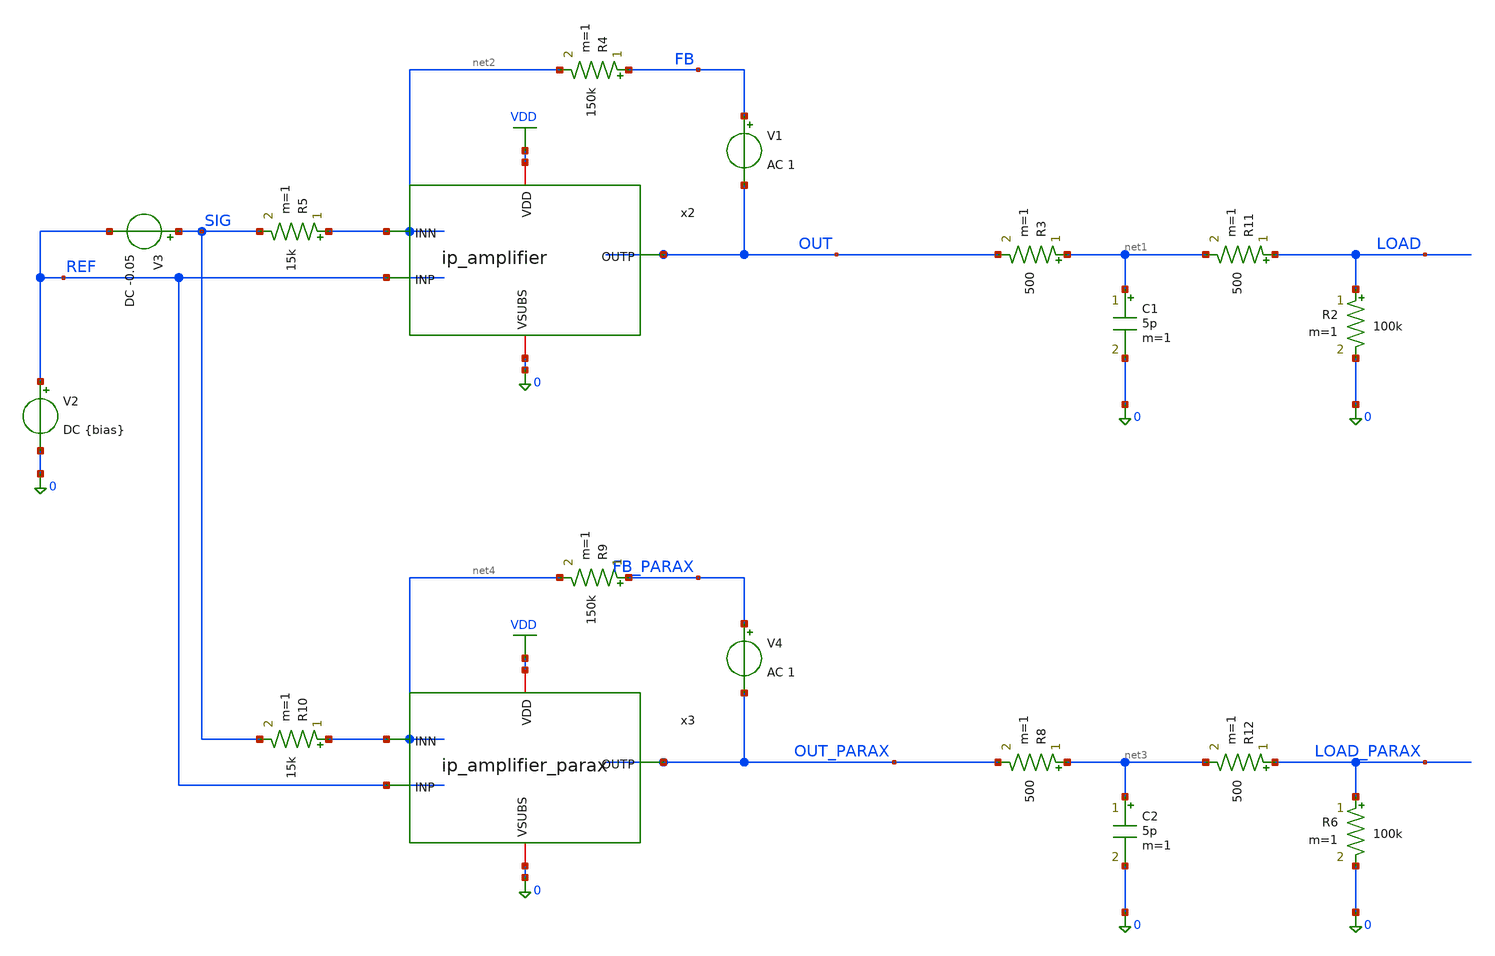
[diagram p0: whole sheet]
** sch_path: xschem/tb_amplifier_x10_ac.sch
**.subckt tb_amplifier_x10_ac
V2 REF 0 DC {bias}
x2 VDD OUT REF net2 0 ip_amplifier
R2 LOAD 0 100k m=1
V1 FB OUT AC 1
R3 net1 OUT 500 m=1
C1 net1 0 5p m=1
R4 FB net2 150k m=1
R5 net2 SIG 15k m=1
V3 SIG REF DC -0.05
R6 LOAD_PARAX 0 100k m=1
V4 FB_PARAX OUT_PARAX AC 1
R8 net3 OUT_PARAX 500 m=1
C2 net3 0 5p m=1
R9 FB_PARAX net4 150k m=1
R10 net4 SIG 15k m=1
x3 VDD OUT_PARAX REF net4 0 ip_amplifier_parax
R11 LOAD net1 500 m=1
R12 LOAD_PARAX net3 500 m=1
**** begin user architecture code

.lib $::180MCU_MODELS/sm141064.ngspice statistical
.lib $::180MCU_MODELS/sm141064.ngspice res_statistical
.lib $::180MCU_MODELS/sm141064.ngspice moscap_typical
.lib $::180MCU_MODELS/sm141064.ngspice diode_typical




V_DD VDD 0 3.3

# Global parameters typically sourced from design.ngspice
.param sw_stat_global   = 1
.param sw_stat_mismatch = 1
.param mc_skew          = 1
.param res_mc_skew=3
.param cap_mc_skew=3
.param fnoicor=0

.param bias=1.0

.control
	op
	write tb_amplifier_x10_ac.op.raw
  	foreach v_bias 0.5 1.0 1.5
    		alterparam bias=$v_bias
		repeat 10
			mc_source
			ac dec 1000 1000 1e9
			let oltf = v(out) / v(fb)
			let oltf_parax = v(out_parax) / v(fb_parax)
			write tb_amplifier_x10_ac.raw
			set appendwrite
			reset
		end
	end
	quit
.endc



**** end user architecture code
**.ends

* expanding   symbol:  ip_amplifier.sym # of pins=5
** sym_path: xschem/ip_amplifier.sym
** sch_path: xschem/ip_amplifier.sch
.subckt ip_amplifier VDD OUTP INP INN VSUBS
*.iopin VDD
*.iopin VSUBS
*.ipin INP
*.ipin INN
*.opin OUTP
XM1 net10 INP net8 VDD pfet_06v0 L=0.7u W=11.0u nf=1 ad='int((nf+1)/2) * W/nf * 0.18u' as='int((nf+2)/2) * W/nf * 0.18u'
+ pd='2*int((nf+1)/2) * (W/nf + 0.18u)' ps='2*int((nf+2)/2) * (W/nf + 0.18u)' nrd='0.18u / W' nrs='0.18u / W'
+ sa=0 sb=0 sd=0 m=2 par=2
XM2 net9 INN net8 VDD pfet_06v0 L=0.7u W=11.0u nf=1 ad='int((nf+1)/2) * W/nf * 0.18u' as='int((nf+2)/2) * W/nf * 0.18u'
+ pd='2*int((nf+1)/2) * (W/nf + 0.18u)' ps='2*int((nf+2)/2) * (W/nf + 0.18u)' nrd='0.18u / W' nrs='0.18u / W'
+ sa=0 sb=0 sd=0 m=2 par=2
XM5 net10 net1 VSUBS vsubs nfet_06v0 L=2u W=5u nf=1 ad='int((nf+1)/2) * W/nf * 0.18u' as='int((nf+2)/2) * W/nf * 0.18u'
+ pd='2*int((nf+1)/2) * (W/nf + 0.18u)' ps='2*int((nf+2)/2) * (W/nf + 0.18u)' nrd='0.18u / W' nrs='0.18u / W'
+ sa=0 sb=0 sd=0 m=1 par=1
XM6 net9 net1 VSUBS vsubs nfet_06v0 L=2u W=5u nf=1 ad='int((nf+1)/2) * W/nf * 0.18u' as='int((nf+2)/2) * W/nf * 0.18u'
+ pd='2*int((nf+1)/2) * (W/nf + 0.18u)' ps='2*int((nf+2)/2) * (W/nf + 0.18u)' nrd='0.18u / W' nrs='0.18u / W'
+ sa=0 sb=0 sd=0 m=1 par=1
XM3 net3 net1 VSUBS vsubs nfet_06v0 L=1u W=12.5u nf=1 ad='int((nf+1)/2) * W/nf * 0.18u' as='int((nf+2)/2) * W/nf * 0.18u'
+ pd='2*int((nf+1)/2) * (W/nf + 0.18u)' ps='2*int((nf+2)/2) * (W/nf + 0.18u)' nrd='0.18u / W' nrs='0.18u / W'
+ sa=0 sb=0 sd=0 m=2 par=2
XM4 net2 net1 VSUBS vsubs nfet_06v0 L=1u W=5u nf=1 ad='int((nf+1)/2) * W/nf * 0.18u' as='int((nf+2)/2) * W/nf * 0.18u'
+ pd='2*int((nf+1)/2) * (W/nf + 0.18u)' ps='2*int((nf+2)/2) * (W/nf + 0.18u)' nrd='0.18u / W' nrs='0.18u / W'
+ sa=0 sb=0 sd=0 m=1 par=1
XM7 net1 net1 net3 vsubs nfet_06v0 L=0.7u W=14u nf=1 ad='int((nf+1)/2) * W/nf * 0.18u' as='int((nf+2)/2) * W/nf * 0.18u'
+ pd='2*int((nf+1)/2) * (W/nf + 0.18u)' ps='2*int((nf+2)/2) * (W/nf + 0.18u)' nrd='0.18u / W' nrs='0.18u / W'
+ sa=0 sb=0 sd=0 m=2 par=2
XM8 net4 net1 net2 vsubs nfet_06v0 L=0.7u W=14u nf=1 ad='int((nf+1)/2) * W/nf * 0.18u' as='int((nf+2)/2) * W/nf * 0.18u'
+ pd='2*int((nf+1)/2) * (W/nf + 0.18u)' ps='2*int((nf+2)/2) * (W/nf + 0.18u)' nrd='0.18u / W' nrs='0.18u / W'
+ sa=0 sb=0 sd=0 m=2 par=2
XM9 net5 net7 VDD VDD pfet_06v0 L=1u W=6u nf=1 ad='int((nf+1)/2) * W/nf * 0.18u' as='int((nf+2)/2) * W/nf * 0.18u'
+ pd='2*int((nf+1)/2) * (W/nf + 0.18u)' ps='2*int((nf+2)/2) * (W/nf + 0.18u)' nrd='0.18u / W' nrs='0.18u / W'
+ sa=0 sb=0 sd=0 m=1 par=1
XM10 net6 net7 VDD VDD pfet_06v0 L=1u W=6u nf=1 ad='int((nf+1)/2) * W/nf * 0.18u' as='int((nf+2)/2) * W/nf * 0.18u'
+ pd='2*int((nf+1)/2) * (W/nf + 0.18u)' ps='2*int((nf+2)/2) * (W/nf + 0.18u)' nrd='0.18u / W' nrs='0.18u / W'
+ sa=0 sb=0 sd=0 m=1 par=1
XM11 net7 net7 net5 VDD pfet_06v0 L=0.7u W=14u nf=1 ad='int((nf+1)/2) * W/nf * 0.18u' as='int((nf+2)/2) * W/nf * 0.18u'
+ pd='2*int((nf+1)/2) * (W/nf + 0.18u)' ps='2*int((nf+2)/2) * (W/nf + 0.18u)' nrd='0.18u / W' nrs='0.18u / W'
+ sa=0 sb=0 sd=0 m=2 par=2
XM12 net8 net7 net6 VDD pfet_06v0 L=0.7u W=14u nf=1 ad='int((nf+1)/2) * W/nf * 0.18u' as='int((nf+2)/2) * W/nf * 0.18u'
+ pd='2*int((nf+1)/2) * (W/nf + 0.18u)' ps='2*int((nf+2)/2) * (W/nf + 0.18u)' nrd='0.18u / W' nrs='0.18u / W'
+ sa=0 sb=0 sd=0 m=2 par=2
XM13 net11 net1 net9 vsubs nfet_06v0 L=0.7u W=12u nf=1 ad='int((nf+1)/2) * W/nf * 0.18u' as='int((nf+2)/2) * W/nf * 0.18u'
+ pd='2*int((nf+1)/2) * (W/nf + 0.18u)' ps='2*int((nf+2)/2) * (W/nf + 0.18u)' nrd='0.18u / W' nrs='0.18u / W'
+ sa=0 sb=0 sd=0 m=1 par=1
XM14 COMP net1 net10 vsubs nfet_06v0 L=0.7u W=12u nf=1 ad='int((nf+1)/2) * W/nf * 0.18u' as='int((nf+2)/2) * W/nf * 0.18u'
+ pd='2*int((nf+1)/2) * (W/nf + 0.18u)' ps='2*int((nf+2)/2) * (W/nf + 0.18u)' nrd='0.18u / W' nrs='0.18u / W'
+ sa=0 sb=0 sd=0 m=1 par=1
XM15 net11 net11 VDD VDD pfet_06v0 L=0.7u W=12u nf=1 ad='int((nf+1)/2) * W/nf * 0.18u' as='int((nf+2)/2) * W/nf * 0.18u'
+ pd='2*int((nf+1)/2) * (W/nf + 0.18u)' ps='2*int((nf+2)/2) * (W/nf + 0.18u)' nrd='0.18u / W' nrs='0.18u / W'
+ sa=0 sb=0 sd=0 m=1 par=1
XM16 COMP net11 VDD VDD pfet_06v0 L=0.7u W=12u nf=1 ad='int((nf+1)/2) * W/nf * 0.18u' as='int((nf+2)/2) * W/nf * 0.18u'
+ pd='2*int((nf+1)/2) * (W/nf + 0.18u)' ps='2*int((nf+2)/2) * (W/nf + 0.18u)' nrd='0.18u / W' nrs='0.18u / W'
+ sa=0 sb=0 sd=0 m=1 par=1
XM17 OUTP COMP VDD VDD pfet_06v0 L=0.7u W=12u nf=1 ad='int((nf+1)/2) * W/nf * 0.18u' as='int((nf+2)/2) * W/nf * 0.18u'
+ pd='2*int((nf+1)/2) * (W/nf + 0.18u)' ps='2*int((nf+2)/2) * (W/nf + 0.18u)' nrd='0.18u / W' nrs='0.18u / W'
+ sa=0 sb=0 sd=0 m=5 par=5
XM18 OUTP net10 VSUBS vsubs nfet_06v0 L=0.7u W=12u nf=1 ad='int((nf+1)/2) * W/nf * 0.18u' as='int((nf+2)/2) * W/nf * 0.18u'
+ pd='2*int((nf+1)/2) * (W/nf + 0.18u)' ps='2*int((nf+2)/2) * (W/nf + 0.18u)' nrd='0.18u / W' nrs='0.18u / W'
+ sa=0 sb=0 sd=0 m=3 par=3
XR3 net1 net14 vsubs ppolyf_u_1k_6p0 r_width=1e-6 r_length=6e-6 m=1
XR6 net14 net13 vsubs ppolyf_u_1k_6p0 r_width=1e-6 r_length=6e-6 m=1
XR7 net13 net12 vsubs ppolyf_u_1k_6p0 r_width=1e-6 r_length=6e-6 m=1
XR8 net12 net15 vsubs ppolyf_u_1k_6p0 r_width=1e-6 r_length=4e-6 m=1
Vmeas VDD net15 0
Vmeas1 net7 net4 0
XC1 OUTP net16 cap_nmos_03v3 c_width=12e-6 c_length=18e-6 m=1
XC2 COMP net17 cap_nmos_03v3 c_width=12e-6 c_length=18e-6 m=1
XR12 net16 COMP vsubs ppolyf_u_1k_6p0 r_width=1e-6 r_length=10e-6 m=1
XR16 OUTP net17 vsubs ppolyf_u_1k_6p0 r_width=1e-6 r_length=10e-6 m=1
.ends


* expanding   symbol:  ip_amplifier_parax.sym # of pins=5
** sym_path: xschem/ip_amplifier.sym
.include [file normalize ./parax/ip_amplifier.sim.spice]
.GLOBAL VDD
.end
